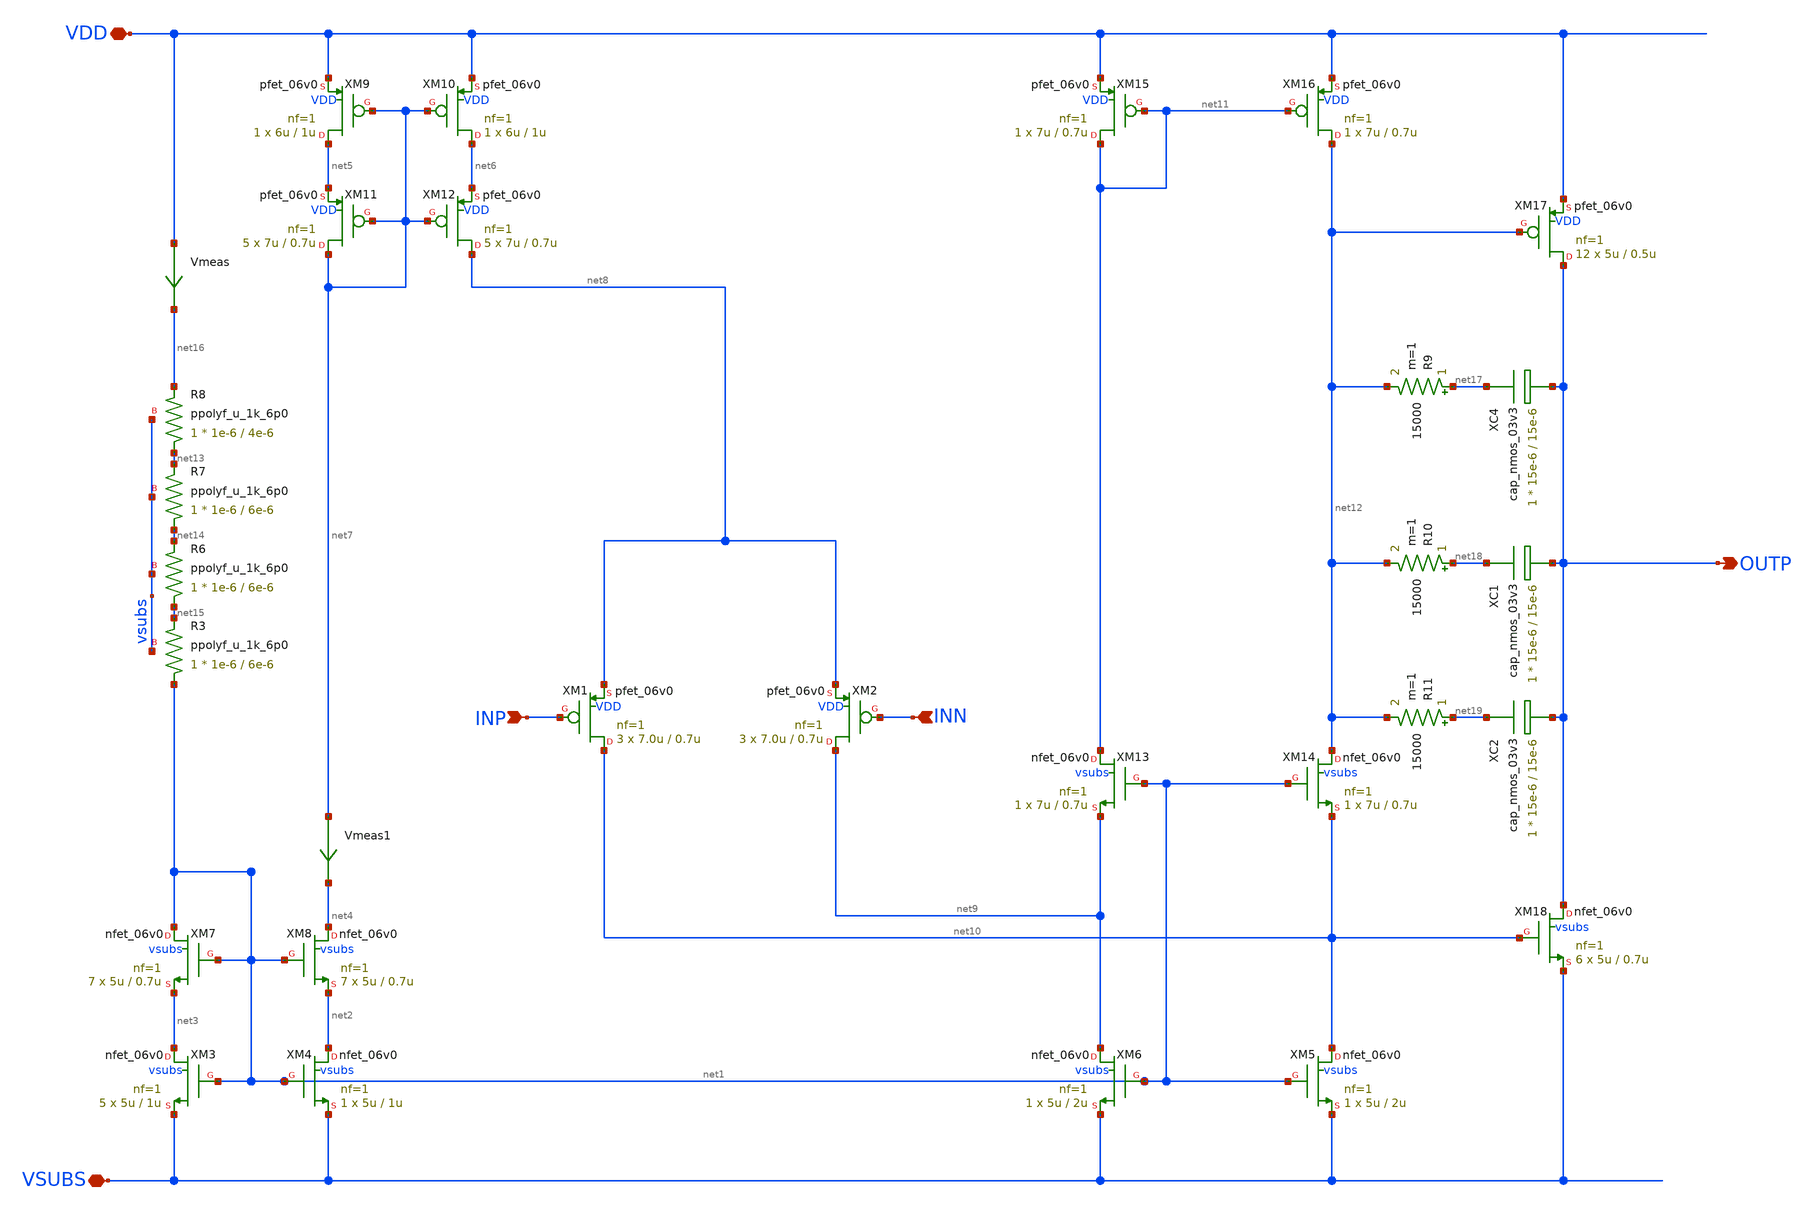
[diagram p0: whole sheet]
** sch_path: xschem/ip_amplifier.sch
**.subckt ip_amplifier VDD VSUBS INP INN OUTP
*.iopin VDD
*.iopin VSUBS
*.ipin INP
*.ipin INN
*.opin OUTP
XM1 net10 INP net8 VDD pfet_06v0 L=0.7u W=7.0u nf=1 ad='int((nf+1)/2) * W/nf * 0.18u' as='int((nf+2)/2) * W/nf * 0.18u'
+ pd='2*int((nf+1)/2) * (W/nf + 0.18u)' ps='2*int((nf+2)/2) * (W/nf + 0.18u)' nrd='0.18u / W' nrs='0.18u / W'
+ sa=0 sb=0 sd=0 m=3 par=3
XM2 net9 INN net8 VDD pfet_06v0 L=0.7u W=7.0u nf=1 ad='int((nf+1)/2) * W/nf * 0.18u' as='int((nf+2)/2) * W/nf * 0.18u'
+ pd='2*int((nf+1)/2) * (W/nf + 0.18u)' ps='2*int((nf+2)/2) * (W/nf + 0.18u)' nrd='0.18u / W' nrs='0.18u / W'
+ sa=0 sb=0 sd=0 m=3 par=3
XM5 net10 net1 VSUBS vsubs nfet_06v0 L=2u W=5u nf=1 ad='int((nf+1)/2) * W/nf * 0.18u' as='int((nf+2)/2) * W/nf * 0.18u'
+ pd='2*int((nf+1)/2) * (W/nf + 0.18u)' ps='2*int((nf+2)/2) * (W/nf + 0.18u)' nrd='0.18u / W' nrs='0.18u / W'
+ sa=0 sb=0 sd=0 m=1 par=1
XM6 net9 net1 VSUBS vsubs nfet_06v0 L=2u W=5u nf=1 ad='int((nf+1)/2) * W/nf * 0.18u' as='int((nf+2)/2) * W/nf * 0.18u'
+ pd='2*int((nf+1)/2) * (W/nf + 0.18u)' ps='2*int((nf+2)/2) * (W/nf + 0.18u)' nrd='0.18u / W' nrs='0.18u / W'
+ sa=0 sb=0 sd=0 m=1 par=1
XM3 net3 net1 VSUBS vsubs nfet_06v0 L=1u W=5u nf=1 ad='int((nf+1)/2) * W/nf * 0.18u' as='int((nf+2)/2) * W/nf * 0.18u'
+ pd='2*int((nf+1)/2) * (W/nf + 0.18u)' ps='2*int((nf+2)/2) * (W/nf + 0.18u)' nrd='0.18u / W' nrs='0.18u / W'
+ sa=0 sb=0 sd=0 m=5 par=5
XM4 net2 net1 VSUBS vsubs nfet_06v0 L=1u W=5u nf=1 ad='int((nf+1)/2) * W/nf * 0.18u' as='int((nf+2)/2) * W/nf * 0.18u'
+ pd='2*int((nf+1)/2) * (W/nf + 0.18u)' ps='2*int((nf+2)/2) * (W/nf + 0.18u)' nrd='0.18u / W' nrs='0.18u / W'
+ sa=0 sb=0 sd=0 m=1 par=1
XM7 net1 net1 net3 vsubs nfet_06v0 L=0.7u W=5u nf=1 ad='int((nf+1)/2) * W/nf * 0.18u' as='int((nf+2)/2) * W/nf * 0.18u'
+ pd='2*int((nf+1)/2) * (W/nf + 0.18u)' ps='2*int((nf+2)/2) * (W/nf + 0.18u)' nrd='0.18u / W' nrs='0.18u / W'
+ sa=0 sb=0 sd=0 m=7 par=7
XM8 net4 net1 net2 vsubs nfet_06v0 L=0.7u W=5u nf=1 ad='int((nf+1)/2) * W/nf * 0.18u' as='int((nf+2)/2) * W/nf * 0.18u'
+ pd='2*int((nf+1)/2) * (W/nf + 0.18u)' ps='2*int((nf+2)/2) * (W/nf + 0.18u)' nrd='0.18u / W' nrs='0.18u / W'
+ sa=0 sb=0 sd=0 m=7 par=7
XM9 net5 net7 VDD VDD pfet_06v0 L=1u W=6u nf=1 ad='int((nf+1)/2) * W/nf * 0.18u' as='int((nf+2)/2) * W/nf * 0.18u'
+ pd='2*int((nf+1)/2) * (W/nf + 0.18u)' ps='2*int((nf+2)/2) * (W/nf + 0.18u)' nrd='0.18u / W' nrs='0.18u / W'
+ sa=0 sb=0 sd=0 m=1 par=1
XM10 net6 net7 VDD VDD pfet_06v0 L=1u W=6u nf=1 ad='int((nf+1)/2) * W/nf * 0.18u' as='int((nf+2)/2) * W/nf * 0.18u'
+ pd='2*int((nf+1)/2) * (W/nf + 0.18u)' ps='2*int((nf+2)/2) * (W/nf + 0.18u)' nrd='0.18u / W' nrs='0.18u / W'
+ sa=0 sb=0 sd=0 m=1 par=1
XM11 net7 net7 net5 VDD pfet_06v0 L=0.7u W=7u nf=1 ad='int((nf+1)/2) * W/nf * 0.18u' as='int((nf+2)/2) * W/nf * 0.18u'
+ pd='2*int((nf+1)/2) * (W/nf + 0.18u)' ps='2*int((nf+2)/2) * (W/nf + 0.18u)' nrd='0.18u / W' nrs='0.18u / W'
+ sa=0 sb=0 sd=0 m=5 par=5
XM12 net8 net7 net6 VDD pfet_06v0 L=0.7u W=7u nf=1 ad='int((nf+1)/2) * W/nf * 0.18u' as='int((nf+2)/2) * W/nf * 0.18u'
+ pd='2*int((nf+1)/2) * (W/nf + 0.18u)' ps='2*int((nf+2)/2) * (W/nf + 0.18u)' nrd='0.18u / W' nrs='0.18u / W'
+ sa=0 sb=0 sd=0 m=5 par=5
XM13 net11 net1 net9 vsubs nfet_06v0 L=0.7u W=7u nf=1 ad='int((nf+1)/2) * W/nf * 0.18u' as='int((nf+2)/2) * W/nf * 0.18u'
+ pd='2*int((nf+1)/2) * (W/nf + 0.18u)' ps='2*int((nf+2)/2) * (W/nf + 0.18u)' nrd='0.18u / W' nrs='0.18u / W'
+ sa=0 sb=0 sd=0 m=1 par=1
XM14 net12 net1 net10 vsubs nfet_06v0 L=0.7u W=7u nf=1 ad='int((nf+1)/2) * W/nf * 0.18u' as='int((nf+2)/2) * W/nf * 0.18u'
+ pd='2*int((nf+1)/2) * (W/nf + 0.18u)' ps='2*int((nf+2)/2) * (W/nf + 0.18u)' nrd='0.18u / W' nrs='0.18u / W'
+ sa=0 sb=0 sd=0 m=1 par=1
XM15 net11 net11 VDD VDD pfet_06v0 L=0.7u W=7u nf=1 ad='int((nf+1)/2) * W/nf * 0.18u' as='int((nf+2)/2) * W/nf * 0.18u'
+ pd='2*int((nf+1)/2) * (W/nf + 0.18u)' ps='2*int((nf+2)/2) * (W/nf + 0.18u)' nrd='0.18u / W' nrs='0.18u / W'
+ sa=0 sb=0 sd=0 m=1 par=1
XM16 net12 net11 VDD VDD pfet_06v0 L=0.7u W=7u nf=1 ad='int((nf+1)/2) * W/nf * 0.18u' as='int((nf+2)/2) * W/nf * 0.18u'
+ pd='2*int((nf+1)/2) * (W/nf + 0.18u)' ps='2*int((nf+2)/2) * (W/nf + 0.18u)' nrd='0.18u / W' nrs='0.18u / W'
+ sa=0 sb=0 sd=0 m=1 par=1
XM17 OUTP net12 VDD VDD pfet_06v0 L=0.5u W=5u nf=1 ad='int((nf+1)/2) * W/nf * 0.18u' as='int((nf+2)/2) * W/nf * 0.18u'
+ pd='2*int((nf+1)/2) * (W/nf + 0.18u)' ps='2*int((nf+2)/2) * (W/nf + 0.18u)' nrd='0.18u / W' nrs='0.18u / W'
+ sa=0 sb=0 sd=0 m=12 par=12
XM18 OUTP net10 VSUBS vsubs nfet_06v0 L=0.7u W=5u nf=1 ad='int((nf+1)/2) * W/nf * 0.18u' as='int((nf+2)/2) * W/nf * 0.18u'
+ pd='2*int((nf+1)/2) * (W/nf + 0.18u)' ps='2*int((nf+2)/2) * (W/nf + 0.18u)' nrd='0.18u / W' nrs='0.18u / W'
+ sa=0 sb=0 sd=0 m=6 par=6
XR3 net1 net15 vsubs ppolyf_u_1k_6p0 r_width=1e-6 r_length=6e-6 m=1
XR6 net15 net14 vsubs ppolyf_u_1k_6p0 r_width=1e-6 r_length=6e-6 m=1
XR7 net14 net13 vsubs ppolyf_u_1k_6p0 r_width=1e-6 r_length=6e-6 m=1
XR8 net13 net16 vsubs ppolyf_u_1k_6p0 r_width=1e-6 r_length=4e-6 m=1
Vmeas VDD net16 0
Vmeas1 net7 net4 0
XC4 net17 OUTP cap_nmos_03v3 c_width=15e-6 c_length=15e-6 m=1
XC1 net18 OUTP cap_nmos_03v3 c_width=15e-6 c_length=15e-6 m=1
XC2 net19 OUTP cap_nmos_03v3 c_width=15e-6 c_length=15e-6 m=1
R9 net17 net12 15000 m=1
R10 net18 net12 15000 m=1
R11 net19 net12 15000 m=1
**.ends
.end
